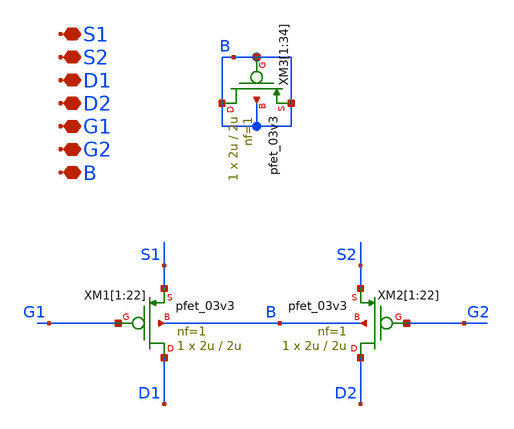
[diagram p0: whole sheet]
** sch_path: Voltage_Reference/LDO/Folded/FC_pfets.sch
**.subckt FC_pfets S1 S2 D1 D2 G1 G2 B
*.iopin S1
*.iopin S2
*.iopin D1
*.iopin D2
*.iopin G1
*.iopin G2
*.iopin B
XM1[1] D1 G1 S1 B pfet_03v3 L=2u W=2u nf=1 ad='int((nf+1)/2) * W/nf * 0.18u' as='int((nf+2)/2) * W/nf * 0.18u'
+ pd='2*int((nf+1)/2) * (W/nf + 0.18u)' ps='2*int((nf+2)/2) * (W/nf + 0.18u)' nrd='0.18u / W' nrs='0.18u / W'
+ sa=0 sb=0 sd=0 m=1
XM1[2] D1 G1 S1 B pfet_03v3 L=2u W=2u nf=1 ad='int((nf+1)/2) * W/nf * 0.18u' as='int((nf+2)/2) * W/nf * 0.18u'
+ pd='2*int((nf+1)/2) * (W/nf + 0.18u)' ps='2*int((nf+2)/2) * (W/nf + 0.18u)' nrd='0.18u / W' nrs='0.18u / W'
+ sa=0 sb=0 sd=0 m=1
XM1[3] D1 G1 S1 B pfet_03v3 L=2u W=2u nf=1 ad='int((nf+1)/2) * W/nf * 0.18u' as='int((nf+2)/2) * W/nf * 0.18u'
+ pd='2*int((nf+1)/2) * (W/nf + 0.18u)' ps='2*int((nf+2)/2) * (W/nf + 0.18u)' nrd='0.18u / W' nrs='0.18u / W'
+ sa=0 sb=0 sd=0 m=1
XM1[4] D1 G1 S1 B pfet_03v3 L=2u W=2u nf=1 ad='int((nf+1)/2) * W/nf * 0.18u' as='int((nf+2)/2) * W/nf * 0.18u'
+ pd='2*int((nf+1)/2) * (W/nf + 0.18u)' ps='2*int((nf+2)/2) * (W/nf + 0.18u)' nrd='0.18u / W' nrs='0.18u / W'
+ sa=0 sb=0 sd=0 m=1
XM1[5] D1 G1 S1 B pfet_03v3 L=2u W=2u nf=1 ad='int((nf+1)/2) * W/nf * 0.18u' as='int((nf+2)/2) * W/nf * 0.18u'
+ pd='2*int((nf+1)/2) * (W/nf + 0.18u)' ps='2*int((nf+2)/2) * (W/nf + 0.18u)' nrd='0.18u / W' nrs='0.18u / W'
+ sa=0 sb=0 sd=0 m=1
XM1[6] D1 G1 S1 B pfet_03v3 L=2u W=2u nf=1 ad='int((nf+1)/2) * W/nf * 0.18u' as='int((nf+2)/2) * W/nf * 0.18u'
+ pd='2*int((nf+1)/2) * (W/nf + 0.18u)' ps='2*int((nf+2)/2) * (W/nf + 0.18u)' nrd='0.18u / W' nrs='0.18u / W'
+ sa=0 sb=0 sd=0 m=1
XM1[7] D1 G1 S1 B pfet_03v3 L=2u W=2u nf=1 ad='int((nf+1)/2) * W/nf * 0.18u' as='int((nf+2)/2) * W/nf * 0.18u'
+ pd='2*int((nf+1)/2) * (W/nf + 0.18u)' ps='2*int((nf+2)/2) * (W/nf + 0.18u)' nrd='0.18u / W' nrs='0.18u / W'
+ sa=0 sb=0 sd=0 m=1
XM1[8] D1 G1 S1 B pfet_03v3 L=2u W=2u nf=1 ad='int((nf+1)/2) * W/nf * 0.18u' as='int((nf+2)/2) * W/nf * 0.18u'
+ pd='2*int((nf+1)/2) * (W/nf + 0.18u)' ps='2*int((nf+2)/2) * (W/nf + 0.18u)' nrd='0.18u / W' nrs='0.18u / W'
+ sa=0 sb=0 sd=0 m=1
XM1[9] D1 G1 S1 B pfet_03v3 L=2u W=2u nf=1 ad='int((nf+1)/2) * W/nf * 0.18u' as='int((nf+2)/2) * W/nf * 0.18u'
+ pd='2*int((nf+1)/2) * (W/nf + 0.18u)' ps='2*int((nf+2)/2) * (W/nf + 0.18u)' nrd='0.18u / W' nrs='0.18u / W'
+ sa=0 sb=0 sd=0 m=1
XM1[10] D1 G1 S1 B pfet_03v3 L=2u W=2u nf=1 ad='int((nf+1)/2) * W/nf * 0.18u' as='int((nf+2)/2) * W/nf * 0.18u'
+ pd='2*int((nf+1)/2) * (W/nf + 0.18u)' ps='2*int((nf+2)/2) * (W/nf + 0.18u)' nrd='0.18u / W' nrs='0.18u / W'
+ sa=0 sb=0 sd=0 m=1
XM1[11] D1 G1 S1 B pfet_03v3 L=2u W=2u nf=1 ad='int((nf+1)/2) * W/nf * 0.18u' as='int((nf+2)/2) * W/nf * 0.18u'
+ pd='2*int((nf+1)/2) * (W/nf + 0.18u)' ps='2*int((nf+2)/2) * (W/nf + 0.18u)' nrd='0.18u / W' nrs='0.18u / W'
+ sa=0 sb=0 sd=0 m=1
XM1[12] D1 G1 S1 B pfet_03v3 L=2u W=2u nf=1 ad='int((nf+1)/2) * W/nf * 0.18u' as='int((nf+2)/2) * W/nf * 0.18u'
+ pd='2*int((nf+1)/2) * (W/nf + 0.18u)' ps='2*int((nf+2)/2) * (W/nf + 0.18u)' nrd='0.18u / W' nrs='0.18u / W'
+ sa=0 sb=0 sd=0 m=1
XM1[13] D1 G1 S1 B pfet_03v3 L=2u W=2u nf=1 ad='int((nf+1)/2) * W/nf * 0.18u' as='int((nf+2)/2) * W/nf * 0.18u'
+ pd='2*int((nf+1)/2) * (W/nf + 0.18u)' ps='2*int((nf+2)/2) * (W/nf + 0.18u)' nrd='0.18u / W' nrs='0.18u / W'
+ sa=0 sb=0 sd=0 m=1
XM1[14] D1 G1 S1 B pfet_03v3 L=2u W=2u nf=1 ad='int((nf+1)/2) * W/nf * 0.18u' as='int((nf+2)/2) * W/nf * 0.18u'
+ pd='2*int((nf+1)/2) * (W/nf + 0.18u)' ps='2*int((nf+2)/2) * (W/nf + 0.18u)' nrd='0.18u / W' nrs='0.18u / W'
+ sa=0 sb=0 sd=0 m=1
XM1[15] D1 G1 S1 B pfet_03v3 L=2u W=2u nf=1 ad='int((nf+1)/2) * W/nf * 0.18u' as='int((nf+2)/2) * W/nf * 0.18u'
+ pd='2*int((nf+1)/2) * (W/nf + 0.18u)' ps='2*int((nf+2)/2) * (W/nf + 0.18u)' nrd='0.18u / W' nrs='0.18u / W'
+ sa=0 sb=0 sd=0 m=1
XM1[16] D1 G1 S1 B pfet_03v3 L=2u W=2u nf=1 ad='int((nf+1)/2) * W/nf * 0.18u' as='int((nf+2)/2) * W/nf * 0.18u'
+ pd='2*int((nf+1)/2) * (W/nf + 0.18u)' ps='2*int((nf+2)/2) * (W/nf + 0.18u)' nrd='0.18u / W' nrs='0.18u / W'
+ sa=0 sb=0 sd=0 m=1
XM1[17] D1 G1 S1 B pfet_03v3 L=2u W=2u nf=1 ad='int((nf+1)/2) * W/nf * 0.18u' as='int((nf+2)/2) * W/nf * 0.18u'
+ pd='2*int((nf+1)/2) * (W/nf + 0.18u)' ps='2*int((nf+2)/2) * (W/nf + 0.18u)' nrd='0.18u / W' nrs='0.18u / W'
+ sa=0 sb=0 sd=0 m=1
XM1[18] D1 G1 S1 B pfet_03v3 L=2u W=2u nf=1 ad='int((nf+1)/2) * W/nf * 0.18u' as='int((nf+2)/2) * W/nf * 0.18u'
+ pd='2*int((nf+1)/2) * (W/nf + 0.18u)' ps='2*int((nf+2)/2) * (W/nf + 0.18u)' nrd='0.18u / W' nrs='0.18u / W'
+ sa=0 sb=0 sd=0 m=1
XM1[19] D1 G1 S1 B pfet_03v3 L=2u W=2u nf=1 ad='int((nf+1)/2) * W/nf * 0.18u' as='int((nf+2)/2) * W/nf * 0.18u'
+ pd='2*int((nf+1)/2) * (W/nf + 0.18u)' ps='2*int((nf+2)/2) * (W/nf + 0.18u)' nrd='0.18u / W' nrs='0.18u / W'
+ sa=0 sb=0 sd=0 m=1
XM1[20] D1 G1 S1 B pfet_03v3 L=2u W=2u nf=1 ad='int((nf+1)/2) * W/nf * 0.18u' as='int((nf+2)/2) * W/nf * 0.18u'
+ pd='2*int((nf+1)/2) * (W/nf + 0.18u)' ps='2*int((nf+2)/2) * (W/nf + 0.18u)' nrd='0.18u / W' nrs='0.18u / W'
+ sa=0 sb=0 sd=0 m=1
XM1[21] D1 G1 S1 B pfet_03v3 L=2u W=2u nf=1 ad='int((nf+1)/2) * W/nf * 0.18u' as='int((nf+2)/2) * W/nf * 0.18u'
+ pd='2*int((nf+1)/2) * (W/nf + 0.18u)' ps='2*int((nf+2)/2) * (W/nf + 0.18u)' nrd='0.18u / W' nrs='0.18u / W'
+ sa=0 sb=0 sd=0 m=1
XM1[22] D1 G1 S1 B pfet_03v3 L=2u W=2u nf=1 ad='int((nf+1)/2) * W/nf * 0.18u' as='int((nf+2)/2) * W/nf * 0.18u'
+ pd='2*int((nf+1)/2) * (W/nf + 0.18u)' ps='2*int((nf+2)/2) * (W/nf + 0.18u)' nrd='0.18u / W' nrs='0.18u / W'
+ sa=0 sb=0 sd=0 m=1
XM2[1] D2 G2 S2 B pfet_03v3 L=2u W=2u nf=1 ad='int((nf+1)/2) * W/nf * 0.18u' as='int((nf+2)/2) * W/nf * 0.18u'
+ pd='2*int((nf+1)/2) * (W/nf + 0.18u)' ps='2*int((nf+2)/2) * (W/nf + 0.18u)' nrd='0.18u / W' nrs='0.18u / W'
+ sa=0 sb=0 sd=0 m=1
XM2[2] D2 G2 S2 B pfet_03v3 L=2u W=2u nf=1 ad='int((nf+1)/2) * W/nf * 0.18u' as='int((nf+2)/2) * W/nf * 0.18u'
+ pd='2*int((nf+1)/2) * (W/nf + 0.18u)' ps='2*int((nf+2)/2) * (W/nf + 0.18u)' nrd='0.18u / W' nrs='0.18u / W'
+ sa=0 sb=0 sd=0 m=1
XM2[3] D2 G2 S2 B pfet_03v3 L=2u W=2u nf=1 ad='int((nf+1)/2) * W/nf * 0.18u' as='int((nf+2)/2) * W/nf * 0.18u'
+ pd='2*int((nf+1)/2) * (W/nf + 0.18u)' ps='2*int((nf+2)/2) * (W/nf + 0.18u)' nrd='0.18u / W' nrs='0.18u / W'
+ sa=0 sb=0 sd=0 m=1
XM2[4] D2 G2 S2 B pfet_03v3 L=2u W=2u nf=1 ad='int((nf+1)/2) * W/nf * 0.18u' as='int((nf+2)/2) * W/nf * 0.18u'
+ pd='2*int((nf+1)/2) * (W/nf + 0.18u)' ps='2*int((nf+2)/2) * (W/nf + 0.18u)' nrd='0.18u / W' nrs='0.18u / W'
+ sa=0 sb=0 sd=0 m=1
XM2[5] D2 G2 S2 B pfet_03v3 L=2u W=2u nf=1 ad='int((nf+1)/2) * W/nf * 0.18u' as='int((nf+2)/2) * W/nf * 0.18u'
+ pd='2*int((nf+1)/2) * (W/nf + 0.18u)' ps='2*int((nf+2)/2) * (W/nf + 0.18u)' nrd='0.18u / W' nrs='0.18u / W'
+ sa=0 sb=0 sd=0 m=1
XM2[6] D2 G2 S2 B pfet_03v3 L=2u W=2u nf=1 ad='int((nf+1)/2) * W/nf * 0.18u' as='int((nf+2)/2) * W/nf * 0.18u'
+ pd='2*int((nf+1)/2) * (W/nf + 0.18u)' ps='2*int((nf+2)/2) * (W/nf + 0.18u)' nrd='0.18u / W' nrs='0.18u / W'
+ sa=0 sb=0 sd=0 m=1
XM2[7] D2 G2 S2 B pfet_03v3 L=2u W=2u nf=1 ad='int((nf+1)/2) * W/nf * 0.18u' as='int((nf+2)/2) * W/nf * 0.18u'
+ pd='2*int((nf+1)/2) * (W/nf + 0.18u)' ps='2*int((nf+2)/2) * (W/nf + 0.18u)' nrd='0.18u / W' nrs='0.18u / W'
+ sa=0 sb=0 sd=0 m=1
XM2[8] D2 G2 S2 B pfet_03v3 L=2u W=2u nf=1 ad='int((nf+1)/2) * W/nf * 0.18u' as='int((nf+2)/2) * W/nf * 0.18u'
+ pd='2*int((nf+1)/2) * (W/nf + 0.18u)' ps='2*int((nf+2)/2) * (W/nf + 0.18u)' nrd='0.18u / W' nrs='0.18u / W'
+ sa=0 sb=0 sd=0 m=1
XM2[9] D2 G2 S2 B pfet_03v3 L=2u W=2u nf=1 ad='int((nf+1)/2) * W/nf * 0.18u' as='int((nf+2)/2) * W/nf * 0.18u'
+ pd='2*int((nf+1)/2) * (W/nf + 0.18u)' ps='2*int((nf+2)/2) * (W/nf + 0.18u)' nrd='0.18u / W' nrs='0.18u / W'
+ sa=0 sb=0 sd=0 m=1
XM2[10] D2 G2 S2 B pfet_03v3 L=2u W=2u nf=1 ad='int((nf+1)/2) * W/nf * 0.18u' as='int((nf+2)/2) * W/nf * 0.18u'
+ pd='2*int((nf+1)/2) * (W/nf + 0.18u)' ps='2*int((nf+2)/2) * (W/nf + 0.18u)' nrd='0.18u / W' nrs='0.18u / W'
+ sa=0 sb=0 sd=0 m=1
XM2[11] D2 G2 S2 B pfet_03v3 L=2u W=2u nf=1 ad='int((nf+1)/2) * W/nf * 0.18u' as='int((nf+2)/2) * W/nf * 0.18u'
+ pd='2*int((nf+1)/2) * (W/nf + 0.18u)' ps='2*int((nf+2)/2) * (W/nf + 0.18u)' nrd='0.18u / W' nrs='0.18u / W'
+ sa=0 sb=0 sd=0 m=1
XM2[12] D2 G2 S2 B pfet_03v3 L=2u W=2u nf=1 ad='int((nf+1)/2) * W/nf * 0.18u' as='int((nf+2)/2) * W/nf * 0.18u'
+ pd='2*int((nf+1)/2) * (W/nf + 0.18u)' ps='2*int((nf+2)/2) * (W/nf + 0.18u)' nrd='0.18u / W' nrs='0.18u / W'
+ sa=0 sb=0 sd=0 m=1
XM2[13] D2 G2 S2 B pfet_03v3 L=2u W=2u nf=1 ad='int((nf+1)/2) * W/nf * 0.18u' as='int((nf+2)/2) * W/nf * 0.18u'
+ pd='2*int((nf+1)/2) * (W/nf + 0.18u)' ps='2*int((nf+2)/2) * (W/nf + 0.18u)' nrd='0.18u / W' nrs='0.18u / W'
+ sa=0 sb=0 sd=0 m=1
XM2[14] D2 G2 S2 B pfet_03v3 L=2u W=2u nf=1 ad='int((nf+1)/2) * W/nf * 0.18u' as='int((nf+2)/2) * W/nf * 0.18u'
+ pd='2*int((nf+1)/2) * (W/nf + 0.18u)' ps='2*int((nf+2)/2) * (W/nf + 0.18u)' nrd='0.18u / W' nrs='0.18u / W'
+ sa=0 sb=0 sd=0 m=1
XM2[15] D2 G2 S2 B pfet_03v3 L=2u W=2u nf=1 ad='int((nf+1)/2) * W/nf * 0.18u' as='int((nf+2)/2) * W/nf * 0.18u'
+ pd='2*int((nf+1)/2) * (W/nf + 0.18u)' ps='2*int((nf+2)/2) * (W/nf + 0.18u)' nrd='0.18u / W' nrs='0.18u / W'
+ sa=0 sb=0 sd=0 m=1
XM2[16] D2 G2 S2 B pfet_03v3 L=2u W=2u nf=1 ad='int((nf+1)/2) * W/nf * 0.18u' as='int((nf+2)/2) * W/nf * 0.18u'
+ pd='2*int((nf+1)/2) * (W/nf + 0.18u)' ps='2*int((nf+2)/2) * (W/nf + 0.18u)' nrd='0.18u / W' nrs='0.18u / W'
+ sa=0 sb=0 sd=0 m=1
XM2[17] D2 G2 S2 B pfet_03v3 L=2u W=2u nf=1 ad='int((nf+1)/2) * W/nf * 0.18u' as='int((nf+2)/2) * W/nf * 0.18u'
+ pd='2*int((nf+1)/2) * (W/nf + 0.18u)' ps='2*int((nf+2)/2) * (W/nf + 0.18u)' nrd='0.18u / W' nrs='0.18u / W'
+ sa=0 sb=0 sd=0 m=1
XM2[18] D2 G2 S2 B pfet_03v3 L=2u W=2u nf=1 ad='int((nf+1)/2) * W/nf * 0.18u' as='int((nf+2)/2) * W/nf * 0.18u'
+ pd='2*int((nf+1)/2) * (W/nf + 0.18u)' ps='2*int((nf+2)/2) * (W/nf + 0.18u)' nrd='0.18u / W' nrs='0.18u / W'
+ sa=0 sb=0 sd=0 m=1
XM2[19] D2 G2 S2 B pfet_03v3 L=2u W=2u nf=1 ad='int((nf+1)/2) * W/nf * 0.18u' as='int((nf+2)/2) * W/nf * 0.18u'
+ pd='2*int((nf+1)/2) * (W/nf + 0.18u)' ps='2*int((nf+2)/2) * (W/nf + 0.18u)' nrd='0.18u / W' nrs='0.18u / W'
+ sa=0 sb=0 sd=0 m=1
XM2[20] D2 G2 S2 B pfet_03v3 L=2u W=2u nf=1 ad='int((nf+1)/2) * W/nf * 0.18u' as='int((nf+2)/2) * W/nf * 0.18u'
+ pd='2*int((nf+1)/2) * (W/nf + 0.18u)' ps='2*int((nf+2)/2) * (W/nf + 0.18u)' nrd='0.18u / W' nrs='0.18u / W'
+ sa=0 sb=0 sd=0 m=1
XM2[21] D2 G2 S2 B pfet_03v3 L=2u W=2u nf=1 ad='int((nf+1)/2) * W/nf * 0.18u' as='int((nf+2)/2) * W/nf * 0.18u'
+ pd='2*int((nf+1)/2) * (W/nf + 0.18u)' ps='2*int((nf+2)/2) * (W/nf + 0.18u)' nrd='0.18u / W' nrs='0.18u / W'
+ sa=0 sb=0 sd=0 m=1
XM2[22] D2 G2 S2 B pfet_03v3 L=2u W=2u nf=1 ad='int((nf+1)/2) * W/nf * 0.18u' as='int((nf+2)/2) * W/nf * 0.18u'
+ pd='2*int((nf+1)/2) * (W/nf + 0.18u)' ps='2*int((nf+2)/2) * (W/nf + 0.18u)' nrd='0.18u / W' nrs='0.18u / W'
+ sa=0 sb=0 sd=0 m=1
XM3[1] B B B B pfet_03v3 L=2u W=2u nf=1 ad='int((nf+1)/2) * W/nf * 0.18u' as='int((nf+2)/2) * W/nf * 0.18u'
+ pd='2*int((nf+1)/2) * (W/nf + 0.18u)' ps='2*int((nf+2)/2) * (W/nf + 0.18u)' nrd='0.18u / W' nrs='0.18u / W'
+ sa=0 sb=0 sd=0 m=1
XM3[2] B B B B pfet_03v3 L=2u W=2u nf=1 ad='int((nf+1)/2) * W/nf * 0.18u' as='int((nf+2)/2) * W/nf * 0.18u'
+ pd='2*int((nf+1)/2) * (W/nf + 0.18u)' ps='2*int((nf+2)/2) * (W/nf + 0.18u)' nrd='0.18u / W' nrs='0.18u / W'
+ sa=0 sb=0 sd=0 m=1
XM3[3] B B B B pfet_03v3 L=2u W=2u nf=1 ad='int((nf+1)/2) * W/nf * 0.18u' as='int((nf+2)/2) * W/nf * 0.18u'
+ pd='2*int((nf+1)/2) * (W/nf + 0.18u)' ps='2*int((nf+2)/2) * (W/nf + 0.18u)' nrd='0.18u / W' nrs='0.18u / W'
+ sa=0 sb=0 sd=0 m=1
XM3[4] B B B B pfet_03v3 L=2u W=2u nf=1 ad='int((nf+1)/2) * W/nf * 0.18u' as='int((nf+2)/2) * W/nf * 0.18u'
+ pd='2*int((nf+1)/2) * (W/nf + 0.18u)' ps='2*int((nf+2)/2) * (W/nf + 0.18u)' nrd='0.18u / W' nrs='0.18u / W'
+ sa=0 sb=0 sd=0 m=1
XM3[5] B B B B pfet_03v3 L=2u W=2u nf=1 ad='int((nf+1)/2) * W/nf * 0.18u' as='int((nf+2)/2) * W/nf * 0.18u'
+ pd='2*int((nf+1)/2) * (W/nf + 0.18u)' ps='2*int((nf+2)/2) * (W/nf + 0.18u)' nrd='0.18u / W' nrs='0.18u / W'
+ sa=0 sb=0 sd=0 m=1
XM3[6] B B B B pfet_03v3 L=2u W=2u nf=1 ad='int((nf+1)/2) * W/nf * 0.18u' as='int((nf+2)/2) * W/nf * 0.18u'
+ pd='2*int((nf+1)/2) * (W/nf + 0.18u)' ps='2*int((nf+2)/2) * (W/nf + 0.18u)' nrd='0.18u / W' nrs='0.18u / W'
+ sa=0 sb=0 sd=0 m=1
XM3[7] B B B B pfet_03v3 L=2u W=2u nf=1 ad='int((nf+1)/2) * W/nf * 0.18u' as='int((nf+2)/2) * W/nf * 0.18u'
+ pd='2*int((nf+1)/2) * (W/nf + 0.18u)' ps='2*int((nf+2)/2) * (W/nf + 0.18u)' nrd='0.18u / W' nrs='0.18u / W'
+ sa=0 sb=0 sd=0 m=1
XM3[8] B B B B pfet_03v3 L=2u W=2u nf=1 ad='int((nf+1)/2) * W/nf * 0.18u' as='int((nf+2)/2) * W/nf * 0.18u'
+ pd='2*int((nf+1)/2) * (W/nf + 0.18u)' ps='2*int((nf+2)/2) * (W/nf + 0.18u)' nrd='0.18u / W' nrs='0.18u / W'
+ sa=0 sb=0 sd=0 m=1
XM3[9] B B B B pfet_03v3 L=2u W=2u nf=1 ad='int((nf+1)/2) * W/nf * 0.18u' as='int((nf+2)/2) * W/nf * 0.18u'
+ pd='2*int((nf+1)/2) * (W/nf + 0.18u)' ps='2*int((nf+2)/2) * (W/nf + 0.18u)' nrd='0.18u / W' nrs='0.18u / W'
+ sa=0 sb=0 sd=0 m=1
XM3[10] B B B B pfet_03v3 L=2u W=2u nf=1 ad='int((nf+1)/2) * W/nf * 0.18u' as='int((nf+2)/2) * W/nf * 0.18u'
+ pd='2*int((nf+1)/2) * (W/nf + 0.18u)' ps='2*int((nf+2)/2) * (W/nf + 0.18u)' nrd='0.18u / W' nrs='0.18u / W'
+ sa=0 sb=0 sd=0 m=1
XM3[11] B B B B pfet_03v3 L=2u W=2u nf=1 ad='int((nf+1)/2) * W/nf * 0.18u' as='int((nf+2)/2) * W/nf * 0.18u'
+ pd='2*int((nf+1)/2) * (W/nf + 0.18u)' ps='2*int((nf+2)/2) * (W/nf + 0.18u)' nrd='0.18u / W' nrs='0.18u / W'
+ sa=0 sb=0 sd=0 m=1
XM3[12] B B B B pfet_03v3 L=2u W=2u nf=1 ad='int((nf+1)/2) * W/nf * 0.18u' as='int((nf+2)/2) * W/nf * 0.18u'
+ pd='2*int((nf+1)/2) * (W/nf + 0.18u)' ps='2*int((nf+2)/2) * (W/nf + 0.18u)' nrd='0.18u / W' nrs='0.18u / W'
+ sa=0 sb=0 sd=0 m=1
XM3[13] B B B B pfet_03v3 L=2u W=2u nf=1 ad='int((nf+1)/2) * W/nf * 0.18u' as='int((nf+2)/2) * W/nf * 0.18u'
+ pd='2*int((nf+1)/2) * (W/nf + 0.18u)' ps='2*int((nf+2)/2) * (W/nf + 0.18u)' nrd='0.18u / W' nrs='0.18u / W'
+ sa=0 sb=0 sd=0 m=1
XM3[14] B B B B pfet_03v3 L=2u W=2u nf=1 ad='int((nf+1)/2) * W/nf * 0.18u' as='int((nf+2)/2) * W/nf * 0.18u'
+ pd='2*int((nf+1)/2) * (W/nf + 0.18u)' ps='2*int((nf+2)/2) * (W/nf + 0.18u)' nrd='0.18u / W' nrs='0.18u / W'
+ sa=0 sb=0 sd=0 m=1
XM3[15] B B B B pfet_03v3 L=2u W=2u nf=1 ad='int((nf+1)/2) * W/nf * 0.18u' as='int((nf+2)/2) * W/nf * 0.18u'
+ pd='2*int((nf+1)/2) * (W/nf + 0.18u)' ps='2*int((nf+2)/2) * (W/nf + 0.18u)' nrd='0.18u / W' nrs='0.18u / W'
+ sa=0 sb=0 sd=0 m=1
XM3[16] B B B B pfet_03v3 L=2u W=2u nf=1 ad='int((nf+1)/2) * W/nf * 0.18u' as='int((nf+2)/2) * W/nf * 0.18u'
+ pd='2*int((nf+1)/2) * (W/nf + 0.18u)' ps='2*int((nf+2)/2) * (W/nf + 0.18u)' nrd='0.18u / W' nrs='0.18u / W'
+ sa=0 sb=0 sd=0 m=1
XM3[17] B B B B pfet_03v3 L=2u W=2u nf=1 ad='int((nf+1)/2) * W/nf * 0.18u' as='int((nf+2)/2) * W/nf * 0.18u'
+ pd='2*int((nf+1)/2) * (W/nf + 0.18u)' ps='2*int((nf+2)/2) * (W/nf + 0.18u)' nrd='0.18u / W' nrs='0.18u / W'
+ sa=0 sb=0 sd=0 m=1
XM3[18] B B B B pfet_03v3 L=2u W=2u nf=1 ad='int((nf+1)/2) * W/nf * 0.18u' as='int((nf+2)/2) * W/nf * 0.18u'
+ pd='2*int((nf+1)/2) * (W/nf + 0.18u)' ps='2*int((nf+2)/2) * (W/nf + 0.18u)' nrd='0.18u / W' nrs='0.18u / W'
+ sa=0 sb=0 sd=0 m=1
XM3[19] B B B B pfet_03v3 L=2u W=2u nf=1 ad='int((nf+1)/2) * W/nf * 0.18u' as='int((nf+2)/2) * W/nf * 0.18u'
+ pd='2*int((nf+1)/2) * (W/nf + 0.18u)' ps='2*int((nf+2)/2) * (W/nf + 0.18u)' nrd='0.18u / W' nrs='0.18u / W'
+ sa=0 sb=0 sd=0 m=1
XM3[20] B B B B pfet_03v3 L=2u W=2u nf=1 ad='int((nf+1)/2) * W/nf * 0.18u' as='int((nf+2)/2) * W/nf * 0.18u'
+ pd='2*int((nf+1)/2) * (W/nf + 0.18u)' ps='2*int((nf+2)/2) * (W/nf + 0.18u)' nrd='0.18u / W' nrs='0.18u / W'
+ sa=0 sb=0 sd=0 m=1
XM3[21] B B B B pfet_03v3 L=2u W=2u nf=1 ad='int((nf+1)/2) * W/nf * 0.18u' as='int((nf+2)/2) * W/nf * 0.18u'
+ pd='2*int((nf+1)/2) * (W/nf + 0.18u)' ps='2*int((nf+2)/2) * (W/nf + 0.18u)' nrd='0.18u / W' nrs='0.18u / W'
+ sa=0 sb=0 sd=0 m=1
XM3[22] B B B B pfet_03v3 L=2u W=2u nf=1 ad='int((nf+1)/2) * W/nf * 0.18u' as='int((nf+2)/2) * W/nf * 0.18u'
+ pd='2*int((nf+1)/2) * (W/nf + 0.18u)' ps='2*int((nf+2)/2) * (W/nf + 0.18u)' nrd='0.18u / W' nrs='0.18u / W'
+ sa=0 sb=0 sd=0 m=1
XM3[23] B B B B pfet_03v3 L=2u W=2u nf=1 ad='int((nf+1)/2) * W/nf * 0.18u' as='int((nf+2)/2) * W/nf * 0.18u'
+ pd='2*int((nf+1)/2) * (W/nf + 0.18u)' ps='2*int((nf+2)/2) * (W/nf + 0.18u)' nrd='0.18u / W' nrs='0.18u / W'
+ sa=0 sb=0 sd=0 m=1
XM3[24] B B B B pfet_03v3 L=2u W=2u nf=1 ad='int((nf+1)/2) * W/nf * 0.18u' as='int((nf+2)/2) * W/nf * 0.18u'
+ pd='2*int((nf+1)/2) * (W/nf + 0.18u)' ps='2*int((nf+2)/2) * (W/nf + 0.18u)' nrd='0.18u / W' nrs='0.18u / W'
+ sa=0 sb=0 sd=0 m=1
XM3[25] B B B B pfet_03v3 L=2u W=2u nf=1 ad='int((nf+1)/2) * W/nf * 0.18u' as='int((nf+2)/2) * W/nf * 0.18u'
+ pd='2*int((nf+1)/2) * (W/nf + 0.18u)' ps='2*int((nf+2)/2) * (W/nf + 0.18u)' nrd='0.18u / W' nrs='0.18u / W'
+ sa=0 sb=0 sd=0 m=1
XM3[26] B B B B pfet_03v3 L=2u W=2u nf=1 ad='int((nf+1)/2) * W/nf * 0.18u' as='int((nf+2)/2) * W/nf * 0.18u'
+ pd='2*int((nf+1)/2) * (W/nf + 0.18u)' ps='2*int((nf+2)/2) * (W/nf + 0.18u)' nrd='0.18u / W' nrs='0.18u / W'
+ sa=0 sb=0 sd=0 m=1
XM3[27] B B B B pfet_03v3 L=2u W=2u nf=1 ad='int((nf+1)/2) * W/nf * 0.18u' as='int((nf+2)/2) * W/nf * 0.18u'
+ pd='2*int((nf+1)/2) * (W/nf + 0.18u)' ps='2*int((nf+2)/2) * (W/nf + 0.18u)' nrd='0.18u / W' nrs='0.18u / W'
+ sa=0 sb=0 sd=0 m=1
XM3[28] B B B B pfet_03v3 L=2u W=2u nf=1 ad='int((nf+1)/2) * W/nf * 0.18u' as='int((nf+2)/2) * W/nf * 0.18u'
+ pd='2*int((nf+1)/2) * (W/nf + 0.18u)' ps='2*int((nf+2)/2) * (W/nf + 0.18u)' nrd='0.18u / W' nrs='0.18u / W'
+ sa=0 sb=0 sd=0 m=1
XM3[29] B B B B pfet_03v3 L=2u W=2u nf=1 ad='int((nf+1)/2) * W/nf * 0.18u' as='int((nf+2)/2) * W/nf * 0.18u'
+ pd='2*int((nf+1)/2) * (W/nf + 0.18u)' ps='2*int((nf+2)/2) * (W/nf + 0.18u)' nrd='0.18u / W' nrs='0.18u / W'
+ sa=0 sb=0 sd=0 m=1
XM3[30] B B B B pfet_03v3 L=2u W=2u nf=1 ad='int((nf+1)/2) * W/nf * 0.18u' as='int((nf+2)/2) * W/nf * 0.18u'
+ pd='2*int((nf+1)/2) * (W/nf + 0.18u)' ps='2*int((nf+2)/2) * (W/nf + 0.18u)' nrd='0.18u / W' nrs='0.18u / W'
+ sa=0 sb=0 sd=0 m=1
XM3[31] B B B B pfet_03v3 L=2u W=2u nf=1 ad='int((nf+1)/2) * W/nf * 0.18u' as='int((nf+2)/2) * W/nf * 0.18u'
+ pd='2*int((nf+1)/2) * (W/nf + 0.18u)' ps='2*int((nf+2)/2) * (W/nf + 0.18u)' nrd='0.18u / W' nrs='0.18u / W'
+ sa=0 sb=0 sd=0 m=1
XM3[32] B B B B pfet_03v3 L=2u W=2u nf=1 ad='int((nf+1)/2) * W/nf * 0.18u' as='int((nf+2)/2) * W/nf * 0.18u'
+ pd='2*int((nf+1)/2) * (W/nf + 0.18u)' ps='2*int((nf+2)/2) * (W/nf + 0.18u)' nrd='0.18u / W' nrs='0.18u / W'
+ sa=0 sb=0 sd=0 m=1
XM3[33] B B B B pfet_03v3 L=2u W=2u nf=1 ad='int((nf+1)/2) * W/nf * 0.18u' as='int((nf+2)/2) * W/nf * 0.18u'
+ pd='2*int((nf+1)/2) * (W/nf + 0.18u)' ps='2*int((nf+2)/2) * (W/nf + 0.18u)' nrd='0.18u / W' nrs='0.18u / W'
+ sa=0 sb=0 sd=0 m=1
XM3[34] B B B B pfet_03v3 L=2u W=2u nf=1 ad='int((nf+1)/2) * W/nf * 0.18u' as='int((nf+2)/2) * W/nf * 0.18u'
+ pd='2*int((nf+1)/2) * (W/nf + 0.18u)' ps='2*int((nf+2)/2) * (W/nf + 0.18u)' nrd='0.18u / W' nrs='0.18u / W'
+ sa=0 sb=0 sd=0 m=1
**.ends
.end
